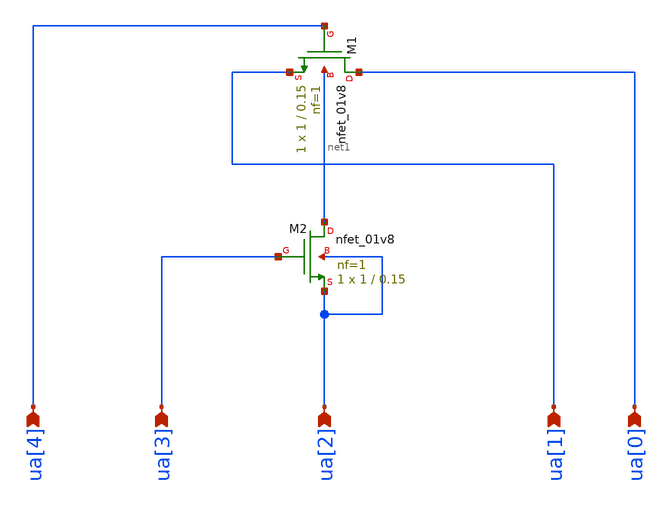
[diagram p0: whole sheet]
** sch_path: xschem/LVS/tt_um_floating_bulk_test_2_NETGEN.sch
**.subckt tt_um_floating_bulk_test_2_NETGEN ua[0] ua[1] ua[2] ua[3] ua[4]
*.ipin ua[0]
*.ipin ua[1]
*.ipin ua[2]
*.ipin ua[3]
*.ipin ua[4]
XM1 ua[0] ua[4] ua[1] net1 sky130_fd_pr__nfet_01v8 L=0.15 W=1 nf=1 ad='int((nf+1)/2) * W/nf * 0.29' as='int((nf+2)/2) * W/nf * 0.29'
+ pd='2*int((nf+1)/2) * (W/nf + 0.29)' ps='2*int((nf+2)/2) * (W/nf + 0.29)' nrd='0.29 / W' nrs='0.29 / W'
+ sa=0 sb=0 sd=0 mult=1 m=1
XM2 net1 ua[3] ua[2] ua[2] sky130_fd_pr__nfet_01v8 L=0.15 W=1 nf=1 ad='int((nf+1)/2) * W/nf * 0.29' as='int((nf+2)/2) * W/nf * 0.29'
+ pd='2*int((nf+1)/2) * (W/nf + 0.29)' ps='2*int((nf+2)/2) * (W/nf + 0.29)' nrd='0.29 / W' nrs='0.29 / W'
+ sa=0 sb=0 sd=0 mult=1 m=1
**.ends
.end
